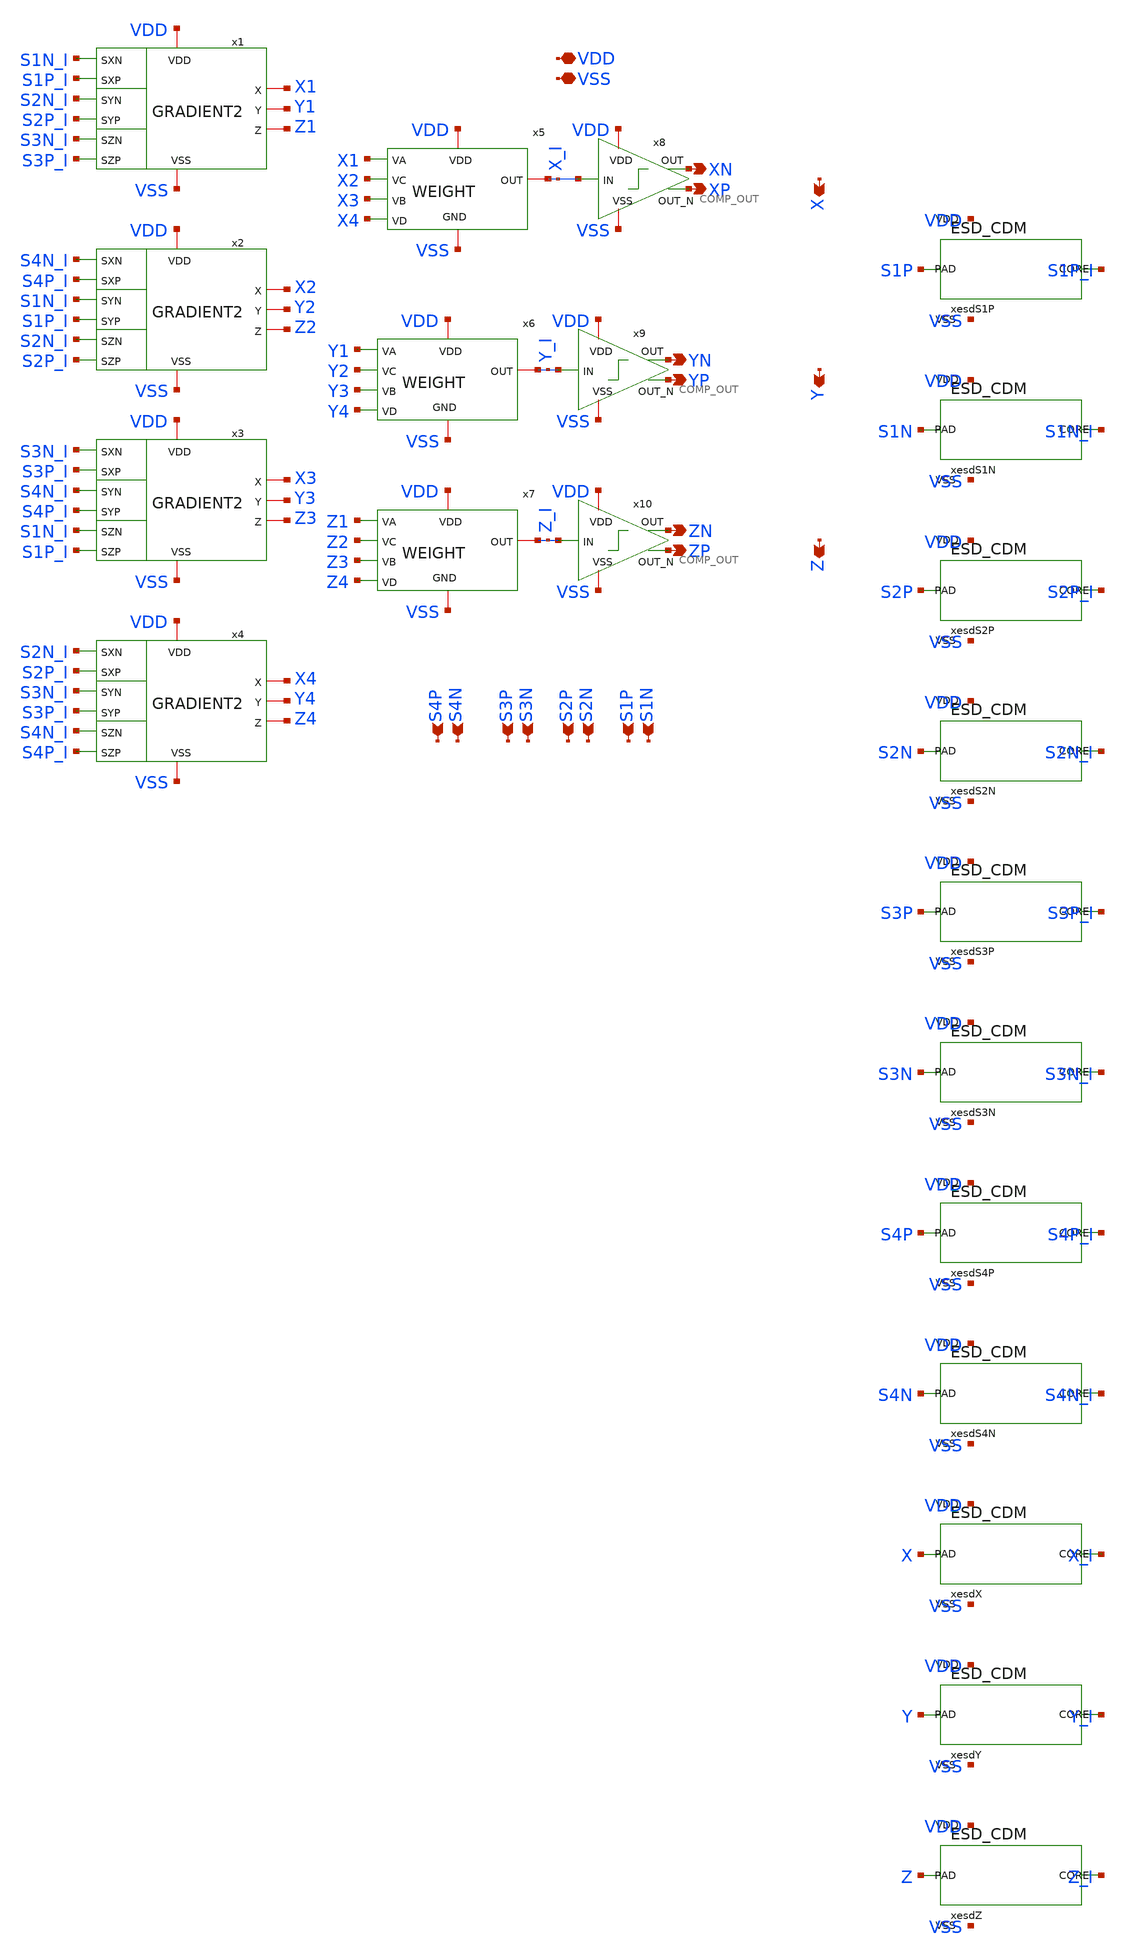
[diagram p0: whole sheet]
** sch_path: FINAL/XSCHEM/GRADIENT_NAV2.sch
**.subckt GRADIENT_NAV2 S1N VDD XP VSS S1P S2N S2P S3N S3P S4N S4P XN YP YN ZP ZN X Y Z
*.ipin S1N
*.iopin VDD
*.opin XP
*.iopin VSS
*.ipin S1P
*.ipin S2N
*.ipin S2P
*.ipin S3N
*.ipin S3P
*.ipin S4N
*.ipin S4P
*.opin XN
*.opin YP
*.opin YN
*.opin ZP
*.opin ZN
*.opin X
*.opin Y
*.opin Z
x5 VDD VSS X_I X1 X2 X3 X4 WEIGHT
x6 VDD VSS Y_I Y1 Y2 Y3 Y4 WEIGHT
x7 VDD VSS Z_I Z1 Z2 Z3 Z4 WEIGHT
x8 VDD XN X_I XP VSS COMP_OUT
x9 VDD YN Y_I YP VSS COMP_OUT
x10 VDD ZN Z_I ZP VSS COMP_OUT
x1 S1N_I S1P_I VDD X1 S2N_I Y1 Z1 S2P_I VSS S3N_I S3P_I GRADIENT2
x2 S4N_I S4P_I VDD X2 S1N_I Y2 Z2 S1P_I VSS S2N_I S2P_I GRADIENT2
x3 S3N_I S3P_I VDD X3 S4N_I Y3 Z3 S4P_I VSS S1N_I S1P_I GRADIENT2
x4 S2N_I S2P_I VDD X4 S3N_I Y4 Z4 S3P_I VSS S4N_I S4P_I GRADIENT2
xesdS1P S1P S1P_I VDD VSS ESD_CDM
xesdS1N S1N S1N_I VDD VSS ESD_CDM
xesdS2P S2P S2P_I VDD VSS ESD_CDM
xesdS2N S2N S2N_I VDD VSS ESD_CDM
xesdS3P S3P S3P_I VDD VSS ESD_CDM
xesdS3N S3N S3N_I VDD VSS ESD_CDM
xesdS4P S4P S4P_I VDD VSS ESD_CDM
xesdS4N S4N S4N_I VDD VSS ESD_CDM
xesdX X X_I VDD VSS ESD_CDM
xesdY Y Y_I VDD VSS ESD_CDM
xesdZ Z Z_I VDD VSS ESD_CDM
**** begin user architecture code


* Decoupling capacitors: NMOS and PMOS in inversion dropped into
* the gaps between macros. WRITTEN BY scripts/decap_fill.py -- do
* not edit by hand: it must be exactly what is in the GDS.
XMdecn0 VSS VDD VSS VSS nfet_06v0 L=2.0u W=1.5u nf=1 m=1
XMdecn1 VSS VDD VSS VSS nfet_06v0 L=2.0u W=1.5u nf=1 m=1
XMdecn2 VSS VDD VSS VSS nfet_06v0 L=2.0u W=1.5u nf=1 m=1
XMdecn3 VSS VDD VSS VSS nfet_06v0 L=2.0u W=1.5u nf=1 m=1
XMdecn4 VSS VDD VSS VSS nfet_06v0 L=2.0u W=1.5u nf=1 m=1
XMdecn5 VSS VDD VSS VSS nfet_06v0 L=2.0u W=1.5u nf=1 m=1
XMdecn6 VSS VDD VSS VSS nfet_06v0 L=2.0u W=1.5u nf=1 m=1
XMdecn7 VSS VDD VSS VSS nfet_06v0 L=2.0u W=1.5u nf=1 m=1
XMdecn8 VSS VDD VSS VSS nfet_06v0 L=2.0u W=1.5u nf=1 m=1
XMdecn9 VSS VDD VSS VSS nfet_06v0 L=2.0u W=1.5u nf=1 m=1
XMdecn10 VSS VDD VSS VSS nfet_06v0 L=2.0u W=1.5u nf=1 m=1
XMdecn11 VSS VDD VSS VSS nfet_06v0 L=2.0u W=1.5u nf=1 m=1
XMdecn12 VSS VDD VSS VSS nfet_06v0 L=2.0u W=1.5u nf=1 m=1
XMdecn13 VSS VDD VSS VSS nfet_06v0 L=2.0u W=1.5u nf=1 m=1
XMdecn14 VSS VDD VSS VSS nfet_06v0 L=2.0u W=1.5u nf=1 m=1
XMdecn15 VSS VDD VSS VSS nfet_06v0 L=2.0u W=1.5u nf=1 m=1
XMdecn16 VSS VDD VSS VSS nfet_06v0 L=2.0u W=1.5u nf=1 m=1
XMdecn17 VSS VDD VSS VSS nfet_06v0 L=2.0u W=1.5u nf=1 m=1
XMdecn18 VSS VDD VSS VSS nfet_06v0 L=2.0u W=1.5u nf=1 m=1
XMdecn19 VSS VDD VSS VSS nfet_06v0 L=2.0u W=1.5u nf=1 m=1
XMdecn20 VSS VDD VSS VSS nfet_06v0 L=2.0u W=1.5u nf=1 m=1
XMdecn21 VSS VDD VSS VSS nfet_06v0 L=2.0u W=1.5u nf=1 m=1
XMdecn22 VSS VDD VSS VSS nfet_06v0 L=2.0u W=1.5u nf=1 m=1
XMdecn23 VSS VDD VSS VSS nfet_06v0 L=2.0u W=1.5u nf=1 m=1
XMdecn24 VSS VDD VSS VSS nfet_06v0 L=2.0u W=1.5u nf=1 m=1
XMdecp25 VDD VSS VDD VDD pfet_06v0 L=2.0u W=1.5u nf=1 m=1
XMdecp26 VDD VSS VDD VDD pfet_06v0 L=2.0u W=1.5u nf=1 m=1
XMdecp27 VDD VSS VDD VDD pfet_06v0 L=2.0u W=1.5u nf=1 m=1
XMdecp28 VDD VSS VDD VDD pfet_06v0 L=2.0u W=1.5u nf=1 m=1
XMdecp29 VDD VSS VDD VDD pfet_06v0 L=2.0u W=1.5u nf=1 m=1
XMdecp30 VDD VSS VDD VDD pfet_06v0 L=2.0u W=1.5u nf=1 m=1
XMdecp31 VDD VSS VDD VDD pfet_06v0 L=2.0u W=1.5u nf=1 m=1
XMdecp32 VDD VSS VDD VDD pfet_06v0 L=2.0u W=1.5u nf=1 m=1
XMdecp33 VDD VSS VDD VDD pfet_06v0 L=2.0u W=1.5u nf=1 m=1
XMdecp34 VDD VSS VDD VDD pfet_06v0 L=2.0u W=1.5u nf=1 m=1
XMdecp35 VDD VSS VDD VDD pfet_06v0 L=2.0u W=1.5u nf=1 m=1
XMdecp36 VDD VSS VDD VDD pfet_06v0 L=2.0u W=1.5u nf=1 m=1
XMdecp37 VDD VSS VDD VDD pfet_06v0 L=2.0u W=1.5u nf=1 m=1
XMdecp38 VDD VSS VDD VDD pfet_06v0 L=2.0u W=1.5u nf=1 m=1
XMdecp39 VDD VSS VDD VDD pfet_06v0 L=2.0u W=1.5u nf=1 m=1
XMdecp40 VDD VSS VDD VDD pfet_06v0 L=2.0u W=1.5u nf=1 m=1
XMdecp41 VDD VSS VDD VDD pfet_06v0 L=2.0u W=1.5u nf=1 m=1
XMdecp42 VDD VSS VDD VDD pfet_06v0 L=2.0u W=1.5u nf=1 m=1
XMdecp43 VDD VSS VDD VDD pfet_06v0 L=2.0u W=1.5u nf=1 m=1
XMdecp44 VDD VSS VDD VDD pfet_06v0 L=2.0u W=1.5u nf=1 m=1
XMdecp45 VDD VSS VDD VDD pfet_06v0 L=2.0u W=1.5u nf=1 m=1
XMdecp46 VDD VSS VDD VDD pfet_06v0 L=2.0u W=1.5u nf=1 m=1
XMdecp47 VDD VSS VDD VDD pfet_06v0 L=2.0u W=1.5u nf=1 m=1
XMdecn48 VSS VDD VSS VSS nfet_06v0 L=2.0u W=18.0u nf=1 m=1
XMdecn49 VSS VDD VSS VSS nfet_06v0 L=2.0u W=18.0u nf=1 m=1
XMdecp50 VDD VSS VDD VDD pfet_06v0 L=2.0u W=18.0u nf=1 m=1
XMdecp51 VDD VSS VDD VDD pfet_06v0 L=2.0u W=18.0u nf=1 m=1
XMdecn52 VSS VDD VSS VSS nfet_06v0 L=2.0u W=18.0u nf=1 m=1
XMdecn53 VSS VDD VSS VSS nfet_06v0 L=2.0u W=18.0u nf=1 m=1
XMdecp54 VDD VSS VDD VDD pfet_06v0 L=2.0u W=18.0u nf=1 m=1
XMdecp55 VDD VSS VDD VDD pfet_06v0 L=2.0u W=18.0u nf=1 m=1
XMdecn56 VSS VDD VSS VSS nfet_06v0 L=2.0u W=18.0u nf=1 m=1
XMdecn57 VSS VDD VSS VSS nfet_06v0 L=2.0u W=18.0u nf=1 m=1
XMdecp58 VDD VSS VDD VDD pfet_06v0 L=2.0u W=18.0u nf=1 m=1
XMdecp59 VDD VSS VDD VDD pfet_06v0 L=2.0u W=18.0u nf=1 m=1
XMdecn60 VSS VDD VSS VSS nfet_06v0 L=2.0u W=18.0u nf=1 m=1
XMdecn61 VSS VDD VSS VSS nfet_06v0 L=2.0u W=18.0u nf=1 m=1
XMdecp62 VDD VSS VDD VDD pfet_06v0 L=2.0u W=18.0u nf=1 m=1
XMdecp63 VDD VSS VDD VDD pfet_06v0 L=2.0u W=18.0u nf=1 m=1
XMdecn64 VSS VDD VSS VSS nfet_06v0 L=2.0u W=18.0u nf=1 m=1
XMdecn65 VSS VDD VSS VSS nfet_06v0 L=2.0u W=18.0u nf=1 m=1
XMdecp66 VDD VSS VDD VDD pfet_06v0 L=2.0u W=18.0u nf=1 m=1
XMdecp67 VDD VSS VDD VDD pfet_06v0 L=2.0u W=18.0u nf=1 m=1
XMdecn68 VSS VDD VSS VSS nfet_06v0 L=2.0u W=18.0u nf=1 m=1
XMdecn69 VSS VDD VSS VSS nfet_06v0 L=2.0u W=18.0u nf=1 m=1
XMdecp70 VDD VSS VDD VDD pfet_06v0 L=2.0u W=18.0u nf=1 m=1
XMdecp71 VDD VSS VDD VDD pfet_06v0 L=2.0u W=18.0u nf=1 m=1
XMdecn72 VSS VDD VSS VSS nfet_06v0 L=2.0u W=18.0u nf=1 m=1
XMdecn73 VSS VDD VSS VSS nfet_06v0 L=2.0u W=18.0u nf=1 m=1
XMdecp74 VDD VSS VDD VDD pfet_06v0 L=2.0u W=18.0u nf=1 m=1
XMdecp75 VDD VSS VDD VDD pfet_06v0 L=2.0u W=18.0u nf=1 m=1
XMdecn76 VSS VDD VSS VSS nfet_06v0 L=2.0u W=18.0u nf=1 m=1
XMdecn77 VSS VDD VSS VSS nfet_06v0 L=2.0u W=18.0u nf=1 m=1
XMdecp78 VDD VSS VDD VDD pfet_06v0 L=2.0u W=18.0u nf=1 m=1
XMdecp79 VDD VSS VDD VDD pfet_06v0 L=2.0u W=18.0u nf=1 m=1
XMdecn80 VSS VDD VSS VSS nfet_06v0 L=2.0u W=18.0u nf=1 m=1
XMdecn81 VSS VDD VSS VSS nfet_06v0 L=2.0u W=18.0u nf=1 m=1
XMdecp82 VDD VSS VDD VDD pfet_06v0 L=2.0u W=18.0u nf=1 m=1
XMdecp83 VDD VSS VDD VDD pfet_06v0 L=2.0u W=18.0u nf=1 m=1
XMdecn84 VSS VDD VSS VSS nfet_06v0 L=2.0u W=2.0u nf=1 m=1
XMdecn85 VSS VDD VSS VSS nfet_06v0 L=2.0u W=2.0u nf=1 m=1
XMdecn86 VSS VDD VSS VSS nfet_06v0 L=2.0u W=2.0u nf=1 m=1
XMdecn87 VSS VDD VSS VSS nfet_06v0 L=2.0u W=2.0u nf=1 m=1
XMdecn88 VSS VDD VSS VSS nfet_06v0 L=2.0u W=2.0u nf=1 m=1
XMdecn89 VSS VDD VSS VSS nfet_06v0 L=2.0u W=2.0u nf=1 m=1
XMdecn90 VSS VDD VSS VSS nfet_06v0 L=2.0u W=2.0u nf=1 m=1
XMdecn91 VSS VDD VSS VSS nfet_06v0 L=2.0u W=2.0u nf=1 m=1
XMdecp92 VDD VSS VDD VDD pfet_06v0 L=2.0u W=2.0u nf=1 m=1
XMdecp93 VDD VSS VDD VDD pfet_06v0 L=2.0u W=2.0u nf=1 m=1
XMdecp94 VDD VSS VDD VDD pfet_06v0 L=2.0u W=2.0u nf=1 m=1
XMdecp95 VDD VSS VDD VDD pfet_06v0 L=2.0u W=2.0u nf=1 m=1
XMdecp96 VDD VSS VDD VDD pfet_06v0 L=2.0u W=2.0u nf=1 m=1
XMdecp97 VDD VSS VDD VDD pfet_06v0 L=2.0u W=2.0u nf=1 m=1
XMdecp98 VDD VSS VDD VDD pfet_06v0 L=2.0u W=2.0u nf=1 m=1
XMdecn99 VSS VDD VSS VSS nfet_06v0 L=2.0u W=18.0u nf=1 m=1
XMdecp100 VDD VSS VDD VDD pfet_06v0 L=2.0u W=18.0u nf=1 m=1
XMdecn101 VSS VDD VSS VSS nfet_06v0 L=2.0u W=18.0u nf=1 m=1
XMdecp102 VDD VSS VDD VDD pfet_06v0 L=2.0u W=18.0u nf=1 m=1
XMdecn103 VSS VDD VSS VSS nfet_06v0 L=2.0u W=18.0u nf=1 m=1
XMdecp104 VDD VSS VDD VDD pfet_06v0 L=2.0u W=18.0u nf=1 m=1
XMdecn105 VSS VDD VSS VSS nfet_06v0 L=2.0u W=9.75u nf=1 m=1
XMdecn106 VSS VDD VSS VSS nfet_06v0 L=2.0u W=9.75u nf=1 m=1
XMdecp107 VDD VSS VDD VDD pfet_06v0 L=2.0u W=9.75u nf=1 m=1
XMdecp108 VDD VSS VDD VDD pfet_06v0 L=2.0u W=9.75u nf=1 m=1
XMdecn109 VSS VDD VSS VSS nfet_06v0 L=2.0u W=9.75u nf=1 m=1
XMdecn110 VSS VDD VSS VSS nfet_06v0 L=2.0u W=9.75u nf=1 m=1
XMdecp111 VDD VSS VDD VDD pfet_06v0 L=2.0u W=9.75u nf=1 m=1
XMdecp112 VDD VSS VDD VDD pfet_06v0 L=2.0u W=9.75u nf=1 m=1
XMdecn113 VSS VDD VSS VSS nfet_06v0 L=2.0u W=9.75u nf=1 m=1
XMdecn114 VSS VDD VSS VSS nfet_06v0 L=2.0u W=9.75u nf=1 m=1
XMdecp115 VDD VSS VDD VDD pfet_06v0 L=2.0u W=9.75u nf=1 m=1
XMdecp116 VDD VSS VDD VDD pfet_06v0 L=2.0u W=9.75u nf=1 m=1
XMdecn117 VSS VDD VSS VSS nfet_06v0 L=2.0u W=9.75u nf=1 m=1
XMdecn118 VSS VDD VSS VSS nfet_06v0 L=2.0u W=9.75u nf=1 m=1
XMdecp119 VDD VSS VDD VDD pfet_06v0 L=2.0u W=9.75u nf=1 m=1
XMdecp120 VDD VSS VDD VDD pfet_06v0 L=2.0u W=9.75u nf=1 m=1
XMdecn121 VSS VDD VSS VSS nfet_06v0 L=2.0u W=9.75u nf=1 m=1
XMdecn122 VSS VDD VSS VSS nfet_06v0 L=2.0u W=9.75u nf=1 m=1
XMdecp123 VDD VSS VDD VDD pfet_06v0 L=2.0u W=9.75u nf=1 m=1
XMdecp124 VDD VSS VDD VDD pfet_06v0 L=2.0u W=9.75u nf=1 m=1
XMdecn125 VSS VDD VSS VSS nfet_06v0 L=2.0u W=9.75u nf=1 m=1
XMdecn126 VSS VDD VSS VSS nfet_06v0 L=2.0u W=9.75u nf=1 m=1
XMdecp127 VDD VSS VDD VDD pfet_06v0 L=2.0u W=9.75u nf=1 m=1
XMdecp128 VDD VSS VDD VDD pfet_06v0 L=2.0u W=9.75u nf=1 m=1
XMdecn129 VSS VDD VSS VSS nfet_06v0 L=2.0u W=9.75u nf=1 m=1
XMdecn130 VSS VDD VSS VSS nfet_06v0 L=2.0u W=9.75u nf=1 m=1
XMdecp131 VDD VSS VDD VDD pfet_06v0 L=2.0u W=9.75u nf=1 m=1
XMdecp132 VDD VSS VDD VDD pfet_06v0 L=2.0u W=9.75u nf=1 m=1
XMdecn133 VSS VDD VSS VSS nfet_06v0 L=2.0u W=9.75u nf=1 m=1
XMdecn134 VSS VDD VSS VSS nfet_06v0 L=2.0u W=9.75u nf=1 m=1
XMdecp135 VDD VSS VDD VDD pfet_06v0 L=2.0u W=9.75u nf=1 m=1
XMdecp136 VDD VSS VDD VDD pfet_06v0 L=2.0u W=9.75u nf=1 m=1
XMdecn137 VSS VDD VSS VSS nfet_06v0 L=2.0u W=9.75u nf=1 m=1
XMdecn138 VSS VDD VSS VSS nfet_06v0 L=2.0u W=9.75u nf=1 m=1
XMdecp139 VDD VSS VDD VDD pfet_06v0 L=2.0u W=9.75u nf=1 m=1
XMdecp140 VDD VSS VDD VDD pfet_06v0 L=2.0u W=9.75u nf=1 m=1
XMdecn141 VSS VDD VSS VSS nfet_06v0 L=2.0u W=9.75u nf=1 m=1
XMdecn142 VSS VDD VSS VSS nfet_06v0 L=2.0u W=9.75u nf=1 m=1
XMdecp143 VDD VSS VDD VDD pfet_06v0 L=2.0u W=9.75u nf=1 m=1
XMdecp144 VDD VSS VDD VDD pfet_06v0 L=2.0u W=9.75u nf=1 m=1
XMdecn145 VSS VDD VSS VSS nfet_06v0 L=2.0u W=9.75u nf=1 m=1
XMdecn146 VSS VDD VSS VSS nfet_06v0 L=2.0u W=9.75u nf=1 m=1
XMdecp147 VDD VSS VDD VDD pfet_06v0 L=2.0u W=9.75u nf=1 m=1
XMdecp148 VDD VSS VDD VDD pfet_06v0 L=2.0u W=9.75u nf=1 m=1
XMdecn149 VSS VDD VSS VSS nfet_06v0 L=2.0u W=9.75u nf=1 m=1
XMdecn150 VSS VDD VSS VSS nfet_06v0 L=2.0u W=9.75u nf=1 m=1
XMdecp151 VDD VSS VDD VDD pfet_06v0 L=2.0u W=9.75u nf=1 m=1
XMdecp152 VDD VSS VDD VDD pfet_06v0 L=2.0u W=9.75u nf=1 m=1
XMdecn153 VSS VDD VSS VSS nfet_06v0 L=2.0u W=2.0u nf=1 m=1
XMdecn154 VSS VDD VSS VSS nfet_06v0 L=2.0u W=2.0u nf=1 m=1
XMdecn155 VSS VDD VSS VSS nfet_06v0 L=2.0u W=2.0u nf=1 m=1
XMdecn156 VSS VDD VSS VSS nfet_06v0 L=2.0u W=2.0u nf=1 m=1
XMdecn157 VSS VDD VSS VSS nfet_06v0 L=2.0u W=2.0u nf=1 m=1
XMdecp158 VDD VSS VDD VDD pfet_06v0 L=2.0u W=2.0u nf=1 m=1
XMdecp159 VDD VSS VDD VDD pfet_06v0 L=2.0u W=2.0u nf=1 m=1
XMdecp160 VDD VSS VDD VDD pfet_06v0 L=2.0u W=2.0u nf=1 m=1
XMdecp161 VDD VSS VDD VDD pfet_06v0 L=2.0u W=2.0u nf=1 m=1
XMdecn162 VSS VDD VSS VSS nfet_06v0 L=2.0u W=18.0u nf=1 m=1
XMdecp163 VDD VSS VDD VDD pfet_06v0 L=2.0u W=18.0u nf=1 m=1
XMdecn164 VSS VDD VSS VSS nfet_06v0 L=2.0u W=18.0u nf=1 m=1
XMdecp165 VDD VSS VDD VDD pfet_06v0 L=2.0u W=18.0u nf=1 m=1
XMdecn166 VSS VDD VSS VSS nfet_06v0 L=2.0u W=18.0u nf=1 m=1
XMdecp167 VDD VSS VDD VDD pfet_06v0 L=2.0u W=18.0u nf=1 m=1
XMdecn168 VSS VDD VSS VSS nfet_06v0 L=2.0u W=9.75u nf=1 m=1
XMdecp169 VDD VSS VDD VDD pfet_06v0 L=2.0u W=9.75u nf=1 m=1
XMdecn170 VSS VDD VSS VSS nfet_06v0 L=2.0u W=9.75u nf=1 m=1
XMdecp171 VDD VSS VDD VDD pfet_06v0 L=2.0u W=9.75u nf=1 m=1
XMdecn172 VSS VDD VSS VSS nfet_06v0 L=2.0u W=9.75u nf=1 m=1
XMdecp173 VDD VSS VDD VDD pfet_06v0 L=2.0u W=9.75u nf=1 m=1
XMdecn174 VSS VDD VSS VSS nfet_06v0 L=2.0u W=9.75u nf=1 m=1
XMdecp175 VDD VSS VDD VDD pfet_06v0 L=2.0u W=9.75u nf=1 m=1
XMdecn176 VSS VDD VSS VSS nfet_06v0 L=2.0u W=2.0u nf=1 m=1
XMdecn177 VSS VDD VSS VSS nfet_06v0 L=2.0u W=2.0u nf=1 m=1
XMdecp178 VDD VSS VDD VDD pfet_06v0 L=2.0u W=2.0u nf=1 m=1
XMdecp179 VDD VSS VDD VDD pfet_06v0 L=2.0u W=2.0u nf=1 m=1
XMdecn180 VSS VDD VSS VSS nfet_06v0 L=2.0u W=2.0u nf=1 m=1
XMdecn181 VSS VDD VSS VSS nfet_06v0 L=2.0u W=2.0u nf=1 m=1
XMdecp182 VDD VSS VDD VDD pfet_06v0 L=2.0u W=2.0u nf=1 m=1
XMdecp183 VDD VSS VDD VDD pfet_06v0 L=2.0u W=2.0u nf=1 m=1
XMdecn184 VSS VDD VSS VSS nfet_06v0 L=2.0u W=2.0u nf=1 m=1
XMdecn185 VSS VDD VSS VSS nfet_06v0 L=2.0u W=2.0u nf=1 m=1
XMdecp186 VDD VSS VDD VDD pfet_06v0 L=2.0u W=2.0u nf=1 m=1
XMdecp187 VDD VSS VDD VDD pfet_06v0 L=2.0u W=2.0u nf=1 m=1
XMdecn188 VSS VDD VSS VSS nfet_06v0 L=2.0u W=2.0u nf=1 m=1
XMdecn189 VSS VDD VSS VSS nfet_06v0 L=2.0u W=2.0u nf=1 m=1
XMdecp190 VDD VSS VDD VDD pfet_06v0 L=2.0u W=2.0u nf=1 m=1
XMdecp191 VDD VSS VDD VDD pfet_06v0 L=2.0u W=2.0u nf=1 m=1
XMdecn192 VSS VDD VSS VSS nfet_06v0 L=2.0u W=2.0u nf=1 m=1
XMdecn193 VSS VDD VSS VSS nfet_06v0 L=2.0u W=2.0u nf=1 m=1
XMdecp194 VDD VSS VDD VDD pfet_06v0 L=2.0u W=2.0u nf=1 m=1
XMdecp195 VDD VSS VDD VDD pfet_06v0 L=2.0u W=2.0u nf=1 m=1
XMdecn196 VSS VDD VSS VSS nfet_06v0 L=2.0u W=2.0u nf=1 m=1
XMdecn197 VSS VDD VSS VSS nfet_06v0 L=2.0u W=2.0u nf=1 m=1
XMdecp198 VDD VSS VDD VDD pfet_06v0 L=2.0u W=2.0u nf=1 m=1
XMdecp199 VDD VSS VDD VDD pfet_06v0 L=2.0u W=2.0u nf=1 m=1
XMdecn200 VSS VDD VSS VSS nfet_06v0 L=2.0u W=2.0u nf=1 m=1
XMdecn201 VSS VDD VSS VSS nfet_06v0 L=2.0u W=2.0u nf=1 m=1
XMdecp202 VDD VSS VDD VDD pfet_06v0 L=2.0u W=2.0u nf=1 m=1
XMdecp203 VDD VSS VDD VDD pfet_06v0 L=2.0u W=2.0u nf=1 m=1
XMdecn204 VSS VDD VSS VSS nfet_06v0 L=2.0u W=2.0u nf=1 m=1
XMdecn205 VSS VDD VSS VSS nfet_06v0 L=2.0u W=2.0u nf=1 m=1
XMdecp206 VDD VSS VDD VDD pfet_06v0 L=2.0u W=2.0u nf=1 m=1
XMdecp207 VDD VSS VDD VDD pfet_06v0 L=2.0u W=2.0u nf=1 m=1
XMdecn208 VSS VDD VSS VSS nfet_06v0 L=2.0u W=1.5u nf=1 m=1
XMdecn209 VSS VDD VSS VSS nfet_06v0 L=2.0u W=1.5u nf=1 m=1
XMdecp210 VDD VSS VDD VDD pfet_06v0 L=2.0u W=1.5u nf=1 m=1
XMdecp211 VDD VSS VDD VDD pfet_06v0 L=2.0u W=1.5u nf=1 m=1
XMdecn212 VSS VDD VSS VSS nfet_06v0 L=2.0u W=2.0u nf=1 m=1
XMdecn213 VSS VDD VSS VSS nfet_06v0 L=2.0u W=2.0u nf=1 m=1
XMdecp214 VDD VSS VDD VDD pfet_06v0 L=2.0u W=2.0u nf=1 m=1
XMdecp215 VDD VSS VDD VDD pfet_06v0 L=2.0u W=2.0u nf=1 m=1
XMdecn216 VSS VDD VSS VSS nfet_06v0 L=2.0u W=1.5u nf=1 m=1
XMdecn217 VSS VDD VSS VSS nfet_06v0 L=2.0u W=1.5u nf=1 m=1
XMdecp218 VDD VSS VDD VDD pfet_06v0 L=2.0u W=1.5u nf=1 m=1
XMdecp219 VDD VSS VDD VDD pfet_06v0 L=2.0u W=1.5u nf=1 m=1
XMdecn220 VSS VDD VSS VSS nfet_06v0 L=2.0u W=1.5u nf=1 m=1
XMdecn221 VSS VDD VSS VSS nfet_06v0 L=2.0u W=1.5u nf=1 m=1
XMdecp222 VDD VSS VDD VDD pfet_06v0 L=2.0u W=1.5u nf=1 m=1
XMdecp223 VDD VSS VDD VDD pfet_06v0 L=2.0u W=1.5u nf=1 m=1
XMdecn224 VSS VDD VSS VSS nfet_06v0 L=2.0u W=2.0u nf=1 m=1
XMdecp225 VDD VSS VDD VDD pfet_06v0 L=2.0u W=2.0u nf=1 m=1
XMdecn226 VSS VDD VSS VSS nfet_06v0 L=2.0u W=2.0u nf=1 m=1
XMdecp227 VDD VSS VDD VDD pfet_06v0 L=2.0u W=2.0u nf=1 m=1


**** end user architecture code
**.ends
.end
